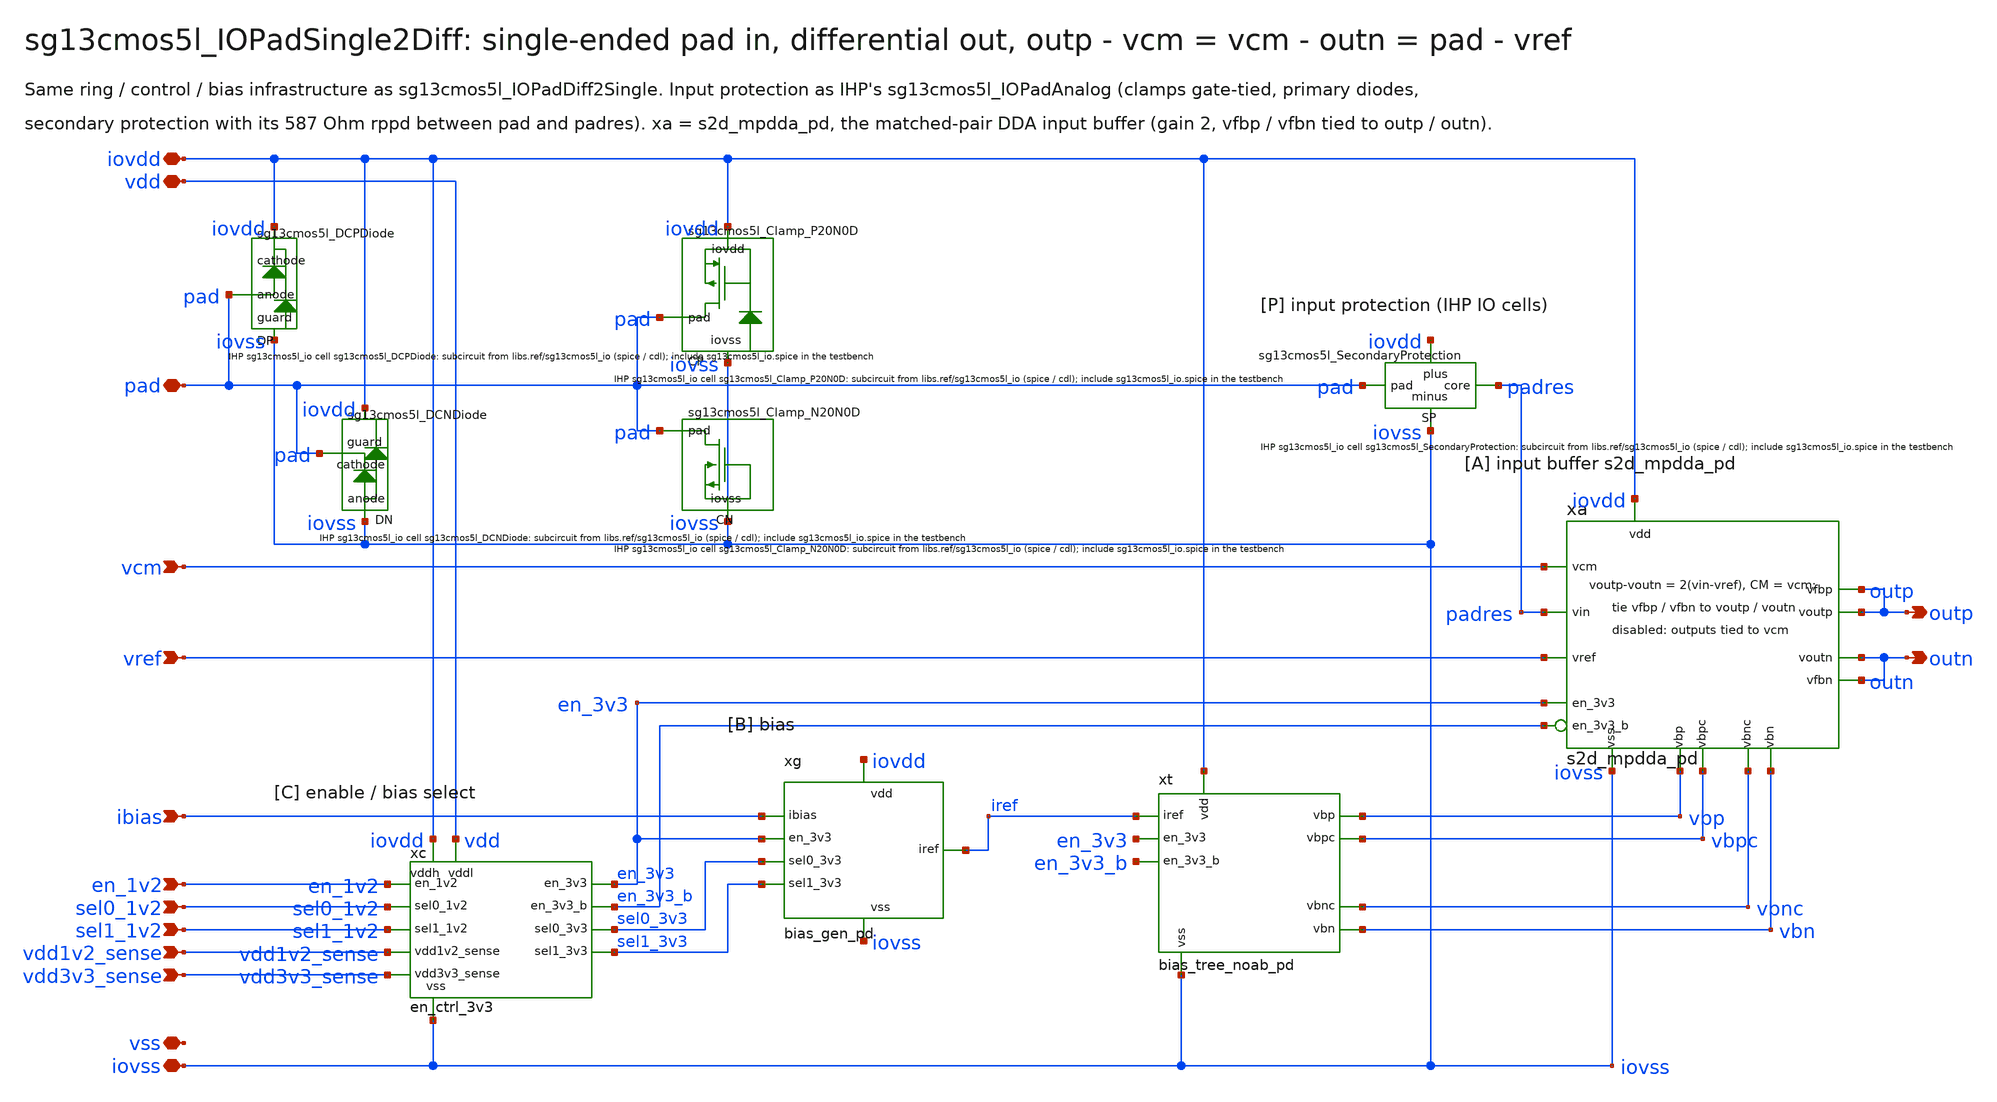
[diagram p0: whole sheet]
** sch_path: sudelbuecher/sg13cmos5l_IOPadSingle2Diff_build/agents_c3/BA/out/macro_before/macros/sg13cmos5l_IOPadSingle2Diff/schematic/xschem/sg13cmos5l_IOPadSingle2Diff.sch
**.subckt sg13cmos5l_IOPadSingle2Diff iovdd iovss vdd vss pad outp outn vcm vref ibias en_1v2
*+ sel0_1v2 sel1_1v2 vdd1v2_sense vdd3v3_sense
*.iopin iovdd
*.iopin iovss
*.iopin vdd
*.iopin vss
*.iopin pad
*.opin outp
*.opin outn
*.ipin vcm
*.ipin vref
*.ipin ibias
*.ipin en_1v2
*.ipin sel0_1v2
*.ipin sel1_1v2
*.ipin vdd1v2_sense
*.ipin vdd3v3_sense
xc iovdd vdd iovss en_1v2 sel0_1v2 sel1_1v2 vdd1v2_sense vdd3v3_sense en_3v3 sel0_3v3 sel1_3v3
+ en_3v3_b en_ctrl_3v3
xa iovdd iovss padres vref vcm outp outn outp outn vbp vbn vbpc vbnc en_3v3 en_3v3_b s2d_mpdda_pd
XCP iovdd iovss pad sg13cmos5l_Clamp_P20N0D
XCN iovss pad sg13cmos5l_Clamp_N20N0D
XDN iovss pad iovdd sg13cmos5l_DCNDiode
XDP pad iovdd iovss sg13cmos5l_DCPDiode
XSP padres iovss pad iovdd sg13cmos5l_SecondaryProtection
xg iovdd iovss ibias iref en_3v3 sel0_3v3 sel1_3v3 bias_gen_pd
xt iovdd iovss iref vbp vbn vbpc vbnc en_3v3 en_3v3_b bias_tree_noab_pd
**.ends
.end
